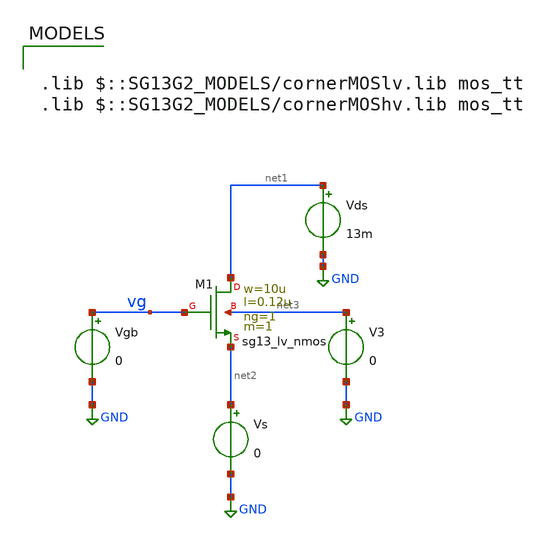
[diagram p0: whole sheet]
** sch_path: legacy/Examples/IHP-SG13/xschem/Extraction/nmos_ext.sch
**.subckt nmos_ext
Vds net1 GND 13m
V3 net3 GND 0
Vs net2 GND 0
Vgb vg GND 0
XM1 net1 vg net2 net3 sg13_lv_nmos w=10u l=0.12u ng=1 m=1 mm_ok=1
**** begin user architecture code



.control
pre_osdi ./psp103_nqs.osdi
save all
save @n.xm1.nsg13_lv_nmos[vto]

dc Vgb 0.02 1.5 1m

let gm_id = deriv(ln(i(Vs)))
save gm_id

meas dc gm_id_max MAX gm_id
let gm_id_vt = 0.531*gm_id_max
save gm_id_vt

meas dc vt0 FIND V(vg) WHEN gm_id=gm_id_vt
meas dc is_ FIND i(Vs) WHEN V(vg)=vt0

let is = is_/0.88
let VT_val=0.026
let n = 1/(gm_id_max*VT_val)
save is vt0 n
echo
echo
echo

echo Extracted parameters:
print is vt0 n


echo
echo
echo

remzerovec
write nmos_ext.raw

.endc




.lib $::SG13G2_MODELS/cornerMOSlv.lib mos_tt
.lib $::SG13G2_MODELS/cornerMOShv.lib mos_tt

**** end user architecture code
**.ends
.GLOBAL GND
.end
